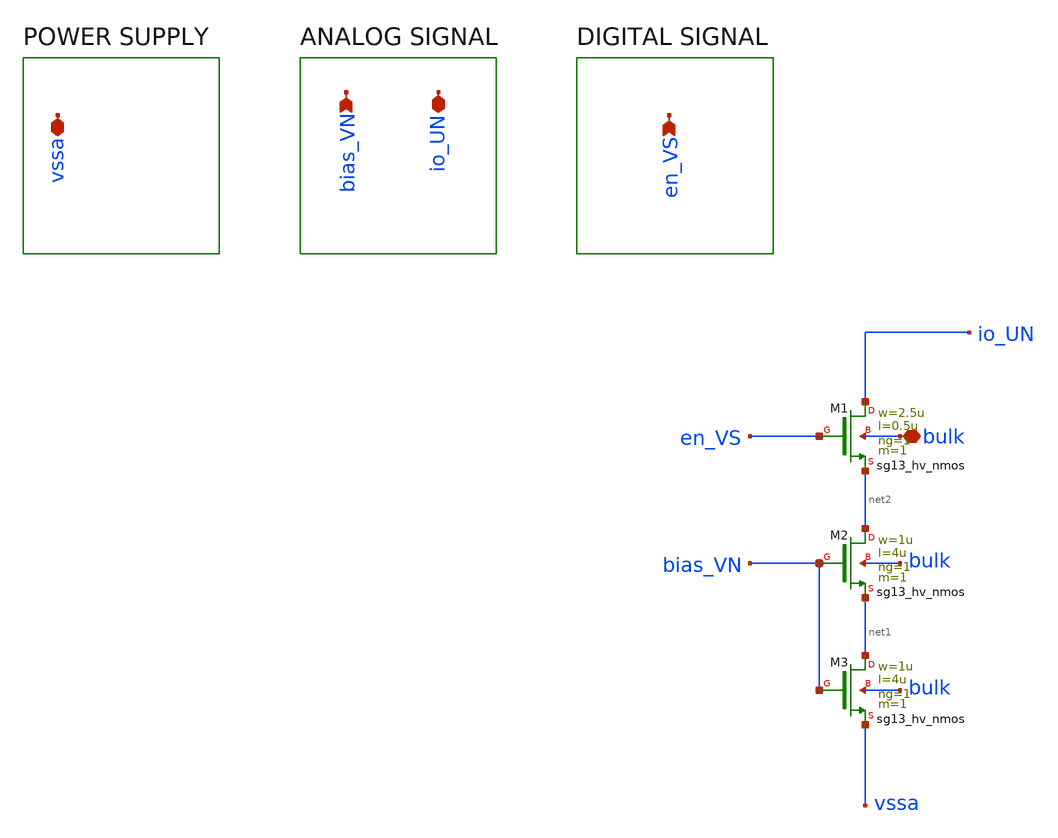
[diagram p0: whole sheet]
** sch_path: ISINK.sch
**.subckt ISINK en_VS vssa bias_VN io_UN bulk
*.ipin en_VS
*.iopin vssa
*.ipin bias_VN
*.iopin io_UN
*.iopin bulk
XM1 io_UN en_VS net2 bulk sg13_hv_nmos w=2.5u l=0.5u ng=1 m=1 mm_ok=1
XM2 net2 bias_VN net1 bulk sg13_hv_nmos w=1u l=4u ng=1 m=1 mm_ok=1
XM3 net1 bias_VN vssa bulk sg13_hv_nmos w=1u l=4u ng=1 m=1 mm_ok=1
**.ends
.end
